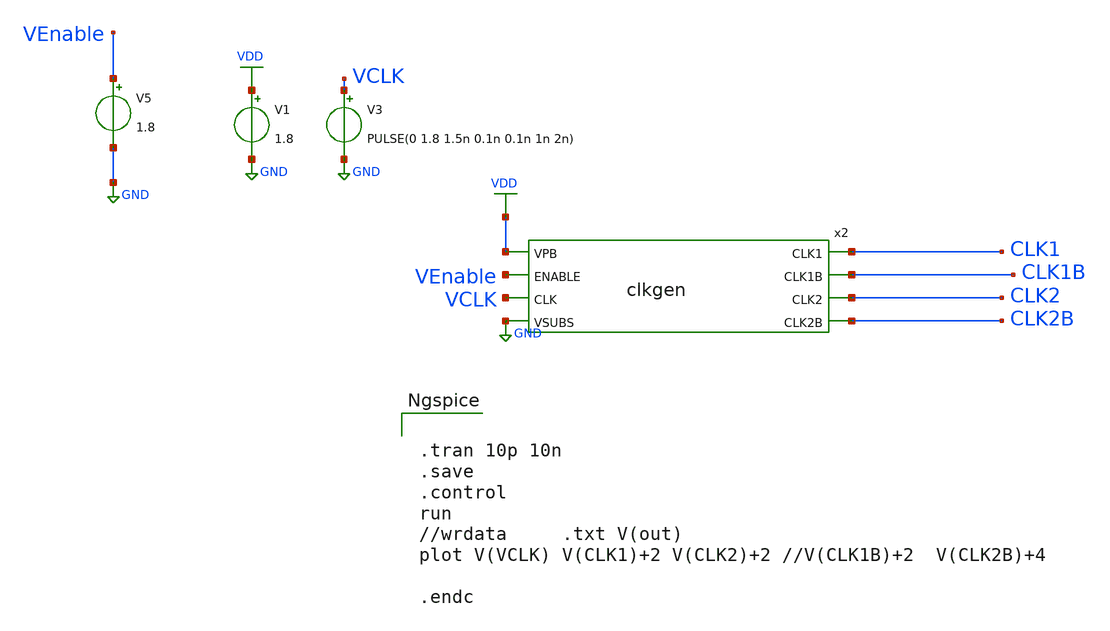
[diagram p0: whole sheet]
** sch_path: sky130_cells/ChargePump/CLKGEN_TB.sch
**.subckt CLKGEN_TB
V3 VCLK GND PULSE(0 1.8 1.5n 0.1n 0.1n 1n 2n)
V1 VDD GND 1.8
V5 VEnable GND 1.8
x2 VDD VEnable VCLK CLK1B CLK1 GND CLK2B CLK2 clkgen
**** begin user architecture code

** opencircuitdesign pdks install
.lib $::SKYWATER_MODELS/sky130.lib.spice tt




.tran 10p 10n
.save
.control
run
//wrdata     .txt V(out)
plot V(VCLK) V(CLK1)+2 V(CLK2)+2 //V(CLK1B)+2  V(CLK2B)+4

.endc



**** end user architecture code
**.ends

* expanding   symbol:  sky130_cells/ChargePump/clkgen.sym # of pins=8
** sym_path: sky130_cells/ChargePump/clkgen.sym
** sch_path: sky130_cells/ChargePump/clkgen.sch
.subckt clkgen VPB ENABLE CLK CLK1B CLK1 VSUBS CLK2B CLK2
*.ipin CLK
*.ipin VPB
*.ipin VSUBS
*.opin CLK1B
*.opin CLK1
*.opin CLK2B
*.opin CLK2
*.ipin ENABLE
XM41 net12 CLK VPB VPB sky130_fd_pr__pfet_01v8_hvt L=0.15 W=1 nf=1 ad='int((1 + 1)/2) * 1 / 1 * 0.29'
+ as='int((1 + 2)/2) * 1 / 1 * 0.29' pd='2*int((1 + 1)/2) * (1 / 1 + 0.29)' ps='2*int((1 + 2)/2) * (1 / 1 + 0.29)'
+ nrd='0.29 / 1 ' nrs='0.29 / 1 ' sa=0 sb=0 sd=0 mult=1 m=1
XM42 net12 ENABLE VPB VPB sky130_fd_pr__pfet_01v8_hvt L=0.15 W=1 nf=1 ad='int((1 + 1)/2) * 1 / 1 * 0.29'
+ as='int((1 + 2)/2) * 1 / 1 * 0.29' pd='2*int((1 + 1)/2) * (1 / 1 + 0.29)' ps='2*int((1 + 2)/2) * (1 / 1 + 0.29)'
+ nrd='0.29 / 1 ' nrs='0.29 / 1 ' sa=0 sb=0 sd=0 mult=1 m=1
XM44 net10 net12 VPB VPB sky130_fd_pr__pfet_01v8_hvt L=0.15 W=1 nf=1 ad='int((1 + 1)/2) * 1 / 1 * 0.29'
+ as='int((1 + 2)/2) * 1 / 1 * 0.29' pd='2*int((1 + 1)/2) * (1 / 1 + 0.29)' ps='2*int((1 + 2)/2) * (1 / 1 + 0.29)'
+ nrd='0.29 / 1 ' nrs='0.29 / 1 ' sa=0 sb=0 sd=0 mult=1 m=1
XM31 net6 A1 VPB VPB sky130_fd_pr__pfet_01v8_hvt L=0.15 W=1 nf=1 ad='int((1 + 1)/2) * 1 / 1 * 0.29' as='int((1 + 2)/2) * 1 / 1 * 0.29'
+ pd='2*int((1 + 1)/2) * (1 / 1 + 0.29)' ps='2*int((1 + 2)/2) * (1 / 1 + 0.29)' nrd='0.29 / 1 ' nrs='0.29 / 1 '
+ sa=0 sb=0 sd=0 mult=1 m=1
XM32 net6 net10 VPB VPB sky130_fd_pr__pfet_01v8_hvt L=0.15 W=1 nf=1 ad='int((1 + 1)/2) * 1 / 1 * 0.29'
+ as='int((1 + 2)/2) * 1 / 1 * 0.29' pd='2*int((1 + 1)/2) * (1 / 1 + 0.29)' ps='2*int((1 + 2)/2) * (1 / 1 + 0.29)'
+ nrd='0.29 / 1 ' nrs='0.29 / 1 ' sa=0 sb=0 sd=0 mult=1 m=1
XM22 p1 net6 VPB VPB sky130_fd_pr__pfet_01v8_hvt L=0.15 W=1 nf=1 ad='int((1 + 1)/2) * 1 / 1 * 0.29' as='int((1 + 2)/2) * 1 / 1 * 0.29'
+ pd='2*int((1 + 1)/2) * (1 / 1 + 0.29)' ps='2*int((1 + 2)/2) * (1 / 1 + 0.29)' nrd='0.29 / 1 ' nrs='0.29 / 1 '
+ sa=0 sb=0 sd=0 mult=3 m=3
XM24 net7 p1 VPB VPB sky130_fd_pr__pfet_01v8_hvt L=0.15 W=1 nf=1 ad='int((1 + 1)/2) * 1 / 1 * 0.29' as='int((1 + 2)/2) * 1 / 1 * 0.29'
+ pd='2*int((1 + 1)/2) * (1 / 1 + 0.29)' ps='2*int((1 + 2)/2) * (1 / 1 + 0.29)' nrd='0.29 / 1 ' nrs='0.29 / 1 '
+ sa=0 sb=0 sd=0 mult=3 m=3
XM26 net8 net7 VPB VPB sky130_fd_pr__pfet_01v8_hvt L=0.15 W=1 nf=1 ad='int((1 + 1)/2) * 1 / 1 * 0.29'
+ as='int((1 + 2)/2) * 1 / 1 * 0.29' pd='2*int((1 + 1)/2) * (1 / 1 + 0.29)' ps='2*int((1 + 2)/2) * (1 / 1 + 0.29)'
+ nrd='0.29 / 1 ' nrs='0.29 / 1 ' sa=0 sb=0 sd=0 mult=3 m=3
XM28 A2 net8 VPB VPB sky130_fd_pr__pfet_01v8_hvt L=0.15 W=1 nf=1 ad='int((1 + 1)/2) * 1 / 1 * 0.29' as='int((1 + 2)/2) * 1 / 1 * 0.29'
+ pd='2*int((1 + 1)/2) * (1 / 1 + 0.29)' ps='2*int((1 + 2)/2) * (1 / 1 + 0.29)' nrd='0.29 / 1 ' nrs='0.29 / 1 '
+ sa=0 sb=0 sd=0 mult=3 m=3
XM2 net1 p1 VPB VPB sky130_fd_pr__pfet_01v8_hvt L=0.15 W=1 nf=1 ad='int((1 + 1)/2) * 1 / 1 * 0.29' as='int((1 + 2)/2) * 1 / 1 * 0.29'
+ pd='2*int((1 + 1)/2) * (1 / 1 + 0.29)' ps='2*int((1 + 2)/2) * (1 / 1 + 0.29)' nrd='0.29 / 1 ' nrs='0.29 / 1 '
+ sa=0 sb=0 sd=0 mult=3 m=3
XM4 CLK1 net1 VPB VPB sky130_fd_pr__pfet_01v8_hvt L=0.15 W=1 nf=1 ad='int((1 + 1)/2) * 1 / 1 * 0.29'
+ as='int((1 + 2)/2) * 1 / 1 * 0.29' pd='2*int((1 + 1)/2) * (1 / 1 + 0.29)' ps='2*int((1 + 2)/2) * (1 / 1 + 0.29)'
+ nrd='0.29 / 1 ' nrs='0.29 / 1 ' sa=0 sb=0 sd=0 mult=3 m=3
XM6 CLK1B CLK1 VPB VPB sky130_fd_pr__pfet_01v8_hvt L=0.15 W=1 nf=1 ad='int((1 + 1)/2) * 1 / 1 * 0.29'
+ as='int((1 + 2)/2) * 1 / 1 * 0.29' pd='2*int((1 + 1)/2) * (1 / 1 + 0.29)' ps='2*int((1 + 2)/2) * (1 / 1 + 0.29)'
+ nrd='0.29 / 1 ' nrs='0.29 / 1 ' sa=0 sb=0 sd=0 mult=3 m=3
XM38 B2 net10 VPB VPB sky130_fd_pr__pfet_01v8_hvt L=0.15 W=1 nf=1 ad='int((1 + 1)/2) * 1 / 1 * 0.29'
+ as='int((1 + 2)/2) * 1 / 1 * 0.29' pd='2*int((1 + 1)/2) * (1 / 1 + 0.29)' ps='2*int((1 + 2)/2) * (1 / 1 + 0.29)'
+ nrd='0.29 / 1 ' nrs='0.29 / 1 ' sa=0 sb=0 sd=0 mult=1 m=1
XM35 net3 A2 VPB VPB sky130_fd_pr__pfet_01v8_hvt L=0.15 W=1 nf=1 ad='int((1 + 1)/2) * 1 / 1 * 0.29' as='int((1 + 2)/2) * 1 / 1 * 0.29'
+ pd='2*int((1 + 1)/2) * (1 / 1 + 0.29)' ps='2*int((1 + 2)/2) * (1 / 1 + 0.29)' nrd='0.29 / 1 ' nrs='0.29 / 1 '
+ sa=0 sb=0 sd=0 mult=1 m=1
XM36 net3 B2 VPB VPB sky130_fd_pr__pfet_01v8_hvt L=0.15 W=1 nf=1 ad='int((1 + 1)/2) * 1 / 1 * 0.29' as='int((1 + 2)/2) * 1 / 1 * 0.29'
+ pd='2*int((1 + 1)/2) * (1 / 1 + 0.29)' ps='2*int((1 + 2)/2) * (1 / 1 + 0.29)' nrd='0.29 / 1 ' nrs='0.29 / 1 '
+ sa=0 sb=0 sd=0 mult=1 m=1
XM14 p2 net3 VPB VPB sky130_fd_pr__pfet_01v8_hvt L=0.15 W=1 nf=1 ad='int((1 + 1)/2) * 1 / 1 * 0.29' as='int((1 + 2)/2) * 1 / 1 * 0.29'
+ pd='2*int((1 + 1)/2) * (1 / 1 + 0.29)' ps='2*int((1 + 2)/2) * (1 / 1 + 0.29)' nrd='0.29 / 1 ' nrs='0.29 / 1 '
+ sa=0 sb=0 sd=0 mult=3 m=3
XM16 net4 p2 VPB VPB sky130_fd_pr__pfet_01v8_hvt L=0.15 W=1 nf=1 ad='int((1 + 1)/2) * 1 / 1 * 0.29' as='int((1 + 2)/2) * 1 / 1 * 0.29'
+ pd='2*int((1 + 1)/2) * (1 / 1 + 0.29)' ps='2*int((1 + 2)/2) * (1 / 1 + 0.29)' nrd='0.29 / 1 ' nrs='0.29 / 1 '
+ sa=0 sb=0 sd=0 mult=3 m=3
XM18 net5 net4 VPB VPB sky130_fd_pr__pfet_01v8_hvt L=0.15 W=1 nf=1 ad='int((1 + 1)/2) * 1 / 1 * 0.29'
+ as='int((1 + 2)/2) * 1 / 1 * 0.29' pd='2*int((1 + 1)/2) * (1 / 1 + 0.29)' ps='2*int((1 + 2)/2) * (1 / 1 + 0.29)'
+ nrd='0.29 / 1 ' nrs='0.29 / 1 ' sa=0 sb=0 sd=0 mult=3 m=3
XM20 A1 net5 VPB VPB sky130_fd_pr__pfet_01v8_hvt L=0.15 W=1 nf=1 ad='int((1 + 1)/2) * 1 / 1 * 0.29' as='int((1 + 2)/2) * 1 / 1 * 0.29'
+ pd='2*int((1 + 1)/2) * (1 / 1 + 0.29)' ps='2*int((1 + 2)/2) * (1 / 1 + 0.29)' nrd='0.29 / 1 ' nrs='0.29 / 1 '
+ sa=0 sb=0 sd=0 mult=3 m=3
XM8 net2 p2 VPB VPB sky130_fd_pr__pfet_01v8_hvt L=0.15 W=1 nf=1 ad='int((1 + 1)/2) * 1 / 1 * 0.29' as='int((1 + 2)/2) * 1 / 1 * 0.29'
+ pd='2*int((1 + 1)/2) * (1 / 1 + 0.29)' ps='2*int((1 + 2)/2) * (1 / 1 + 0.29)' nrd='0.29 / 1 ' nrs='0.29 / 1 '
+ sa=0 sb=0 sd=0 mult=3 m=3
XM10 CLK2 net2 VPB VPB sky130_fd_pr__pfet_01v8_hvt L=0.15 W=1 nf=1 ad='int((1 + 1)/2) * 1 / 1 * 0.29'
+ as='int((1 + 2)/2) * 1 / 1 * 0.29' pd='2*int((1 + 1)/2) * (1 / 1 + 0.29)' ps='2*int((1 + 2)/2) * (1 / 1 + 0.29)'
+ nrd='0.29 / 1 ' nrs='0.29 / 1 ' sa=0 sb=0 sd=0 mult=3 m=3
XM12 CLK2B CLK2 VPB VPB sky130_fd_pr__pfet_01v8_hvt L=0.15 W=1 nf=1 ad='int((1 + 1)/2) * 1 / 1 * 0.29'
+ as='int((1 + 2)/2) * 1 / 1 * 0.29' pd='2*int((1 + 1)/2) * (1 / 1 + 0.29)' ps='2*int((1 + 2)/2) * (1 / 1 + 0.29)'
+ nrd='0.29 / 1 ' nrs='0.29 / 1 ' sa=0 sb=0 sd=0 mult=3 m=3
XM39 net12 ENABLE net13 VSUBS sky130_fd_pr__nfet_01v8 L=0.15 W=0.65 nf=1 ad='int((1 + 1)/2) * 0.65 / 1 * 0.29'
+ as='int((1 + 2)/2) * 0.65 / 1 * 0.29' pd='2*int((1 + 1)/2) * (0.65 / 1 + 0.29)' ps='2*int((1 + 2)/2) * (0.65 / 1 + 0.29)'
+ nrd='0.29 / 0.65 ' nrs='0.29 / 0.65 ' sa=0 sb=0 sd=0 mult=1 m=1
XM40 net13 CLK VSUBS VSUBS sky130_fd_pr__nfet_01v8 L=0.15 W=0.65 nf=1 ad='int((1 + 1)/2) * 0.65 / 1 * 0.29'
+ as='int((1 + 2)/2) * 0.65 / 1 * 0.29' pd='2*int((1 + 1)/2) * (0.65 / 1 + 0.29)' ps='2*int((1 + 2)/2) * (0.65 / 1 + 0.29)'
+ nrd='0.29 / 0.65 ' nrs='0.29 / 0.65 ' sa=0 sb=0 sd=0 mult=1 m=1
XM43 net10 net12 VSUBS VSUBS sky130_fd_pr__nfet_01v8 L=0.15 W=0.65 nf=1 ad='int((1 + 1)/2) * 0.65 / 1 * 0.29'
+ as='int((1 + 2)/2) * 0.65 / 1 * 0.29' pd='2*int((1 + 1)/2) * (0.65 / 1 + 0.29)' ps='2*int((1 + 2)/2) * (0.65 / 1 + 0.29)'
+ nrd='0.29 / 0.65 ' nrs='0.29 / 0.65 ' sa=0 sb=0 sd=0 mult=1 m=1
XM29 net6 A1 net9 VSUBS sky130_fd_pr__nfet_01v8 L=0.15 W=0.65 nf=1 ad='int((1 + 1)/2) * 0.65 / 1 * 0.29'
+ as='int((1 + 2)/2) * 0.65 / 1 * 0.29' pd='2*int((1 + 1)/2) * (0.65 / 1 + 0.29)' ps='2*int((1 + 2)/2) * (0.65 / 1 + 0.29)'
+ nrd='0.29 / 0.65 ' nrs='0.29 / 0.65 ' sa=0 sb=0 sd=0 mult=1 m=1
XM30 net9 net10 VSUBS VSUBS sky130_fd_pr__nfet_01v8 L=0.15 W=0.65 nf=1 ad='int((1 + 1)/2) * 0.65 / 1 * 0.29'
+ as='int((1 + 2)/2) * 0.65 / 1 * 0.29' pd='2*int((1 + 1)/2) * (0.65 / 1 + 0.29)' ps='2*int((1 + 2)/2) * (0.65 / 1 + 0.29)'
+ nrd='0.29 / 0.65 ' nrs='0.29 / 0.65 ' sa=0 sb=0 sd=0 mult=1 m=1
XM21 p1 net6 VSUBS VSUBS sky130_fd_pr__nfet_01v8 L=0.15 W=0.42 nf=1 ad='int((1 + 1)/2) * 0.42 / 1 * 0.29'
+ as='int((1 + 2)/2) * 0.42 / 1 * 0.29' pd='2*int((1 + 1)/2) * (0.42 / 1 + 0.29)' ps='2*int((1 + 2)/2) * (0.42 / 1 + 0.29)'
+ nrd='0.29 / 0.42 ' nrs='0.29 / 0.42 ' sa=0 sb=0 sd=0 mult=2 m=2
XM23 net7 p1 VSUBS VSUBS sky130_fd_pr__nfet_01v8 L=0.15 W=0.42 nf=1 ad='int((1 + 1)/2) * 0.42 / 1 * 0.29'
+ as='int((1 + 2)/2) * 0.42 / 1 * 0.29' pd='2*int((1 + 1)/2) * (0.42 / 1 + 0.29)' ps='2*int((1 + 2)/2) * (0.42 / 1 + 0.29)'
+ nrd='0.29 / 0.42 ' nrs='0.29 / 0.42 ' sa=0 sb=0 sd=0 mult=2 m=2
XM25 net8 net7 VSUBS VSUBS sky130_fd_pr__nfet_01v8 L=0.15 W=0.42 nf=1 ad='int((1 + 1)/2) * 0.42 / 1 * 0.29'
+ as='int((1 + 2)/2) * 0.42 / 1 * 0.29' pd='2*int((1 + 1)/2) * (0.42 / 1 + 0.29)' ps='2*int((1 + 2)/2) * (0.42 / 1 + 0.29)'
+ nrd='0.29 / 0.42 ' nrs='0.29 / 0.42 ' sa=0 sb=0 sd=0 mult=2 m=2
XM27 A2 net8 VSUBS VSUBS sky130_fd_pr__nfet_01v8 L=0.15 W=0.42 nf=1 ad='int((1 + 1)/2) * 0.42 / 1 * 0.29'
+ as='int((1 + 2)/2) * 0.42 / 1 * 0.29' pd='2*int((1 + 1)/2) * (0.42 / 1 + 0.29)' ps='2*int((1 + 2)/2) * (0.42 / 1 + 0.29)'
+ nrd='0.29 / 0.42 ' nrs='0.29 / 0.42 ' sa=0 sb=0 sd=0 mult=2 m=2
XM1 net1 p1 VSUBS VSUBS sky130_fd_pr__nfet_01v8 L=0.15 W=0.42 nf=1 ad='int((1 + 1)/2) * 0.42 / 1 * 0.29'
+ as='int((1 + 2)/2) * 0.42 / 1 * 0.29' pd='2*int((1 + 1)/2) * (0.42 / 1 + 0.29)' ps='2*int((1 + 2)/2) * (0.42 / 1 + 0.29)'
+ nrd='0.29 / 0.42 ' nrs='0.29 / 0.42 ' sa=0 sb=0 sd=0 mult=2 m=2
XM3 CLK1 net1 VSUBS VSUBS sky130_fd_pr__nfet_01v8 L=0.15 W=0.42 nf=1 ad='int((1 + 1)/2) * 0.42 / 1 * 0.29'
+ as='int((1 + 2)/2) * 0.42 / 1 * 0.29' pd='2*int((1 + 1)/2) * (0.42 / 1 + 0.29)' ps='2*int((1 + 2)/2) * (0.42 / 1 + 0.29)'
+ nrd='0.29 / 0.42 ' nrs='0.29 / 0.42 ' sa=0 sb=0 sd=0 mult=2 m=2
XM5 CLK1B CLK1 VSUBS VSUBS sky130_fd_pr__nfet_01v8 L=0.15 W=0.42 nf=1 ad='int((1 + 1)/2) * 0.42 / 1 * 0.29'
+ as='int((1 + 2)/2) * 0.42 / 1 * 0.29' pd='2*int((1 + 1)/2) * (0.42 / 1 + 0.29)' ps='2*int((1 + 2)/2) * (0.42 / 1 + 0.29)'
+ nrd='0.29 / 0.42 ' nrs='0.29 / 0.42 ' sa=0 sb=0 sd=0 mult=2 m=2
XM37 B2 net10 VSUBS VSUBS sky130_fd_pr__nfet_01v8 L=0.15 W=0.65 nf=1 ad='int((1 + 1)/2) * 0.65 / 1 * 0.29'
+ as='int((1 + 2)/2) * 0.65 / 1 * 0.29' pd='2*int((1 + 1)/2) * (0.65 / 1 + 0.29)' ps='2*int((1 + 2)/2) * (0.65 / 1 + 0.29)'
+ nrd='0.29 / 0.65 ' nrs='0.29 / 0.65 ' sa=0 sb=0 sd=0 mult=1 m=1
XM33 net3 A2 net11 VSUBS sky130_fd_pr__nfet_01v8 L=0.15 W=0.65 nf=1 ad='int((1 + 1)/2) * 0.65 / 1 * 0.29'
+ as='int((1 + 2)/2) * 0.65 / 1 * 0.29' pd='2*int((1 + 1)/2) * (0.65 / 1 + 0.29)' ps='2*int((1 + 2)/2) * (0.65 / 1 + 0.29)'
+ nrd='0.29 / 0.65 ' nrs='0.29 / 0.65 ' sa=0 sb=0 sd=0 mult=1 m=1
XM34 net11 B2 VSUBS VSUBS sky130_fd_pr__nfet_01v8 L=0.15 W=0.65 nf=1 ad='int((1 + 1)/2) * 0.65 / 1 * 0.29'
+ as='int((1 + 2)/2) * 0.65 / 1 * 0.29' pd='2*int((1 + 1)/2) * (0.65 / 1 + 0.29)' ps='2*int((1 + 2)/2) * (0.65 / 1 + 0.29)'
+ nrd='0.29 / 0.65 ' nrs='0.29 / 0.65 ' sa=0 sb=0 sd=0 mult=1 m=1
XM13 p2 net3 VSUBS VSUBS sky130_fd_pr__nfet_01v8 L=0.15 W=0.42 nf=1 ad='int((1 + 1)/2) * 0.42 / 1 * 0.29'
+ as='int((1 + 2)/2) * 0.42 / 1 * 0.29' pd='2*int((1 + 1)/2) * (0.42 / 1 + 0.29)' ps='2*int((1 + 2)/2) * (0.42 / 1 + 0.29)'
+ nrd='0.29 / 0.42 ' nrs='0.29 / 0.42 ' sa=0 sb=0 sd=0 mult=2 m=2
XM15 net4 p2 VSUBS VSUBS sky130_fd_pr__nfet_01v8 L=0.15 W=0.42 nf=1 ad='int((1 + 1)/2) * 0.42 / 1 * 0.29'
+ as='int((1 + 2)/2) * 0.42 / 1 * 0.29' pd='2*int((1 + 1)/2) * (0.42 / 1 + 0.29)' ps='2*int((1 + 2)/2) * (0.42 / 1 + 0.29)'
+ nrd='0.29 / 0.42 ' nrs='0.29 / 0.42 ' sa=0 sb=0 sd=0 mult=2 m=2
XM17 net5 net4 VSUBS VSUBS sky130_fd_pr__nfet_01v8 L=0.15 W=0.42 nf=1 ad='int((1 + 1)/2) * 0.42 / 1 * 0.29'
+ as='int((1 + 2)/2) * 0.42 / 1 * 0.29' pd='2*int((1 + 1)/2) * (0.42 / 1 + 0.29)' ps='2*int((1 + 2)/2) * (0.42 / 1 + 0.29)'
+ nrd='0.29 / 0.42 ' nrs='0.29 / 0.42 ' sa=0 sb=0 sd=0 mult=2 m=2
XM19 A1 net5 VSUBS VSUBS sky130_fd_pr__nfet_01v8 L=0.15 W=0.42 nf=1 ad='int((1 + 1)/2) * 0.42 / 1 * 0.29'
+ as='int((1 + 2)/2) * 0.42 / 1 * 0.29' pd='2*int((1 + 1)/2) * (0.42 / 1 + 0.29)' ps='2*int((1 + 2)/2) * (0.42 / 1 + 0.29)'
+ nrd='0.29 / 0.42 ' nrs='0.29 / 0.42 ' sa=0 sb=0 sd=0 mult=2 m=2
XM7 net2 p2 VSUBS VSUBS sky130_fd_pr__nfet_01v8 L=0.15 W=0.42 nf=1 ad='int((1 + 1)/2) * 0.42 / 1 * 0.29'
+ as='int((1 + 2)/2) * 0.42 / 1 * 0.29' pd='2*int((1 + 1)/2) * (0.42 / 1 + 0.29)' ps='2*int((1 + 2)/2) * (0.42 / 1 + 0.29)'
+ nrd='0.29 / 0.42 ' nrs='0.29 / 0.42 ' sa=0 sb=0 sd=0 mult=2 m=2
XM9 CLK2 net2 VSUBS VSUBS sky130_fd_pr__nfet_01v8 L=0.15 W=0.42 nf=1 ad='int((1 + 1)/2) * 0.42 / 1 * 0.29'
+ as='int((1 + 2)/2) * 0.42 / 1 * 0.29' pd='2*int((1 + 1)/2) * (0.42 / 1 + 0.29)' ps='2*int((1 + 2)/2) * (0.42 / 1 + 0.29)'
+ nrd='0.29 / 0.42 ' nrs='0.29 / 0.42 ' sa=0 sb=0 sd=0 mult=2 m=2
XM11 CLK2B CLK2 VSUBS VSUBS sky130_fd_pr__nfet_01v8 L=0.15 W=0.42 nf=1 ad='int((1 + 1)/2) * 0.42 / 1 * 0.29'
+ as='int((1 + 2)/2) * 0.42 / 1 * 0.29' pd='2*int((1 + 1)/2) * (0.42 / 1 + 0.29)' ps='2*int((1 + 2)/2) * (0.42 / 1 + 0.29)'
+ nrd='0.29 / 0.42 ' nrs='0.29 / 0.42 ' sa=0 sb=0 sd=0 mult=2 m=2
.ends

.GLOBAL GND
.GLOBAL VDD
.end
